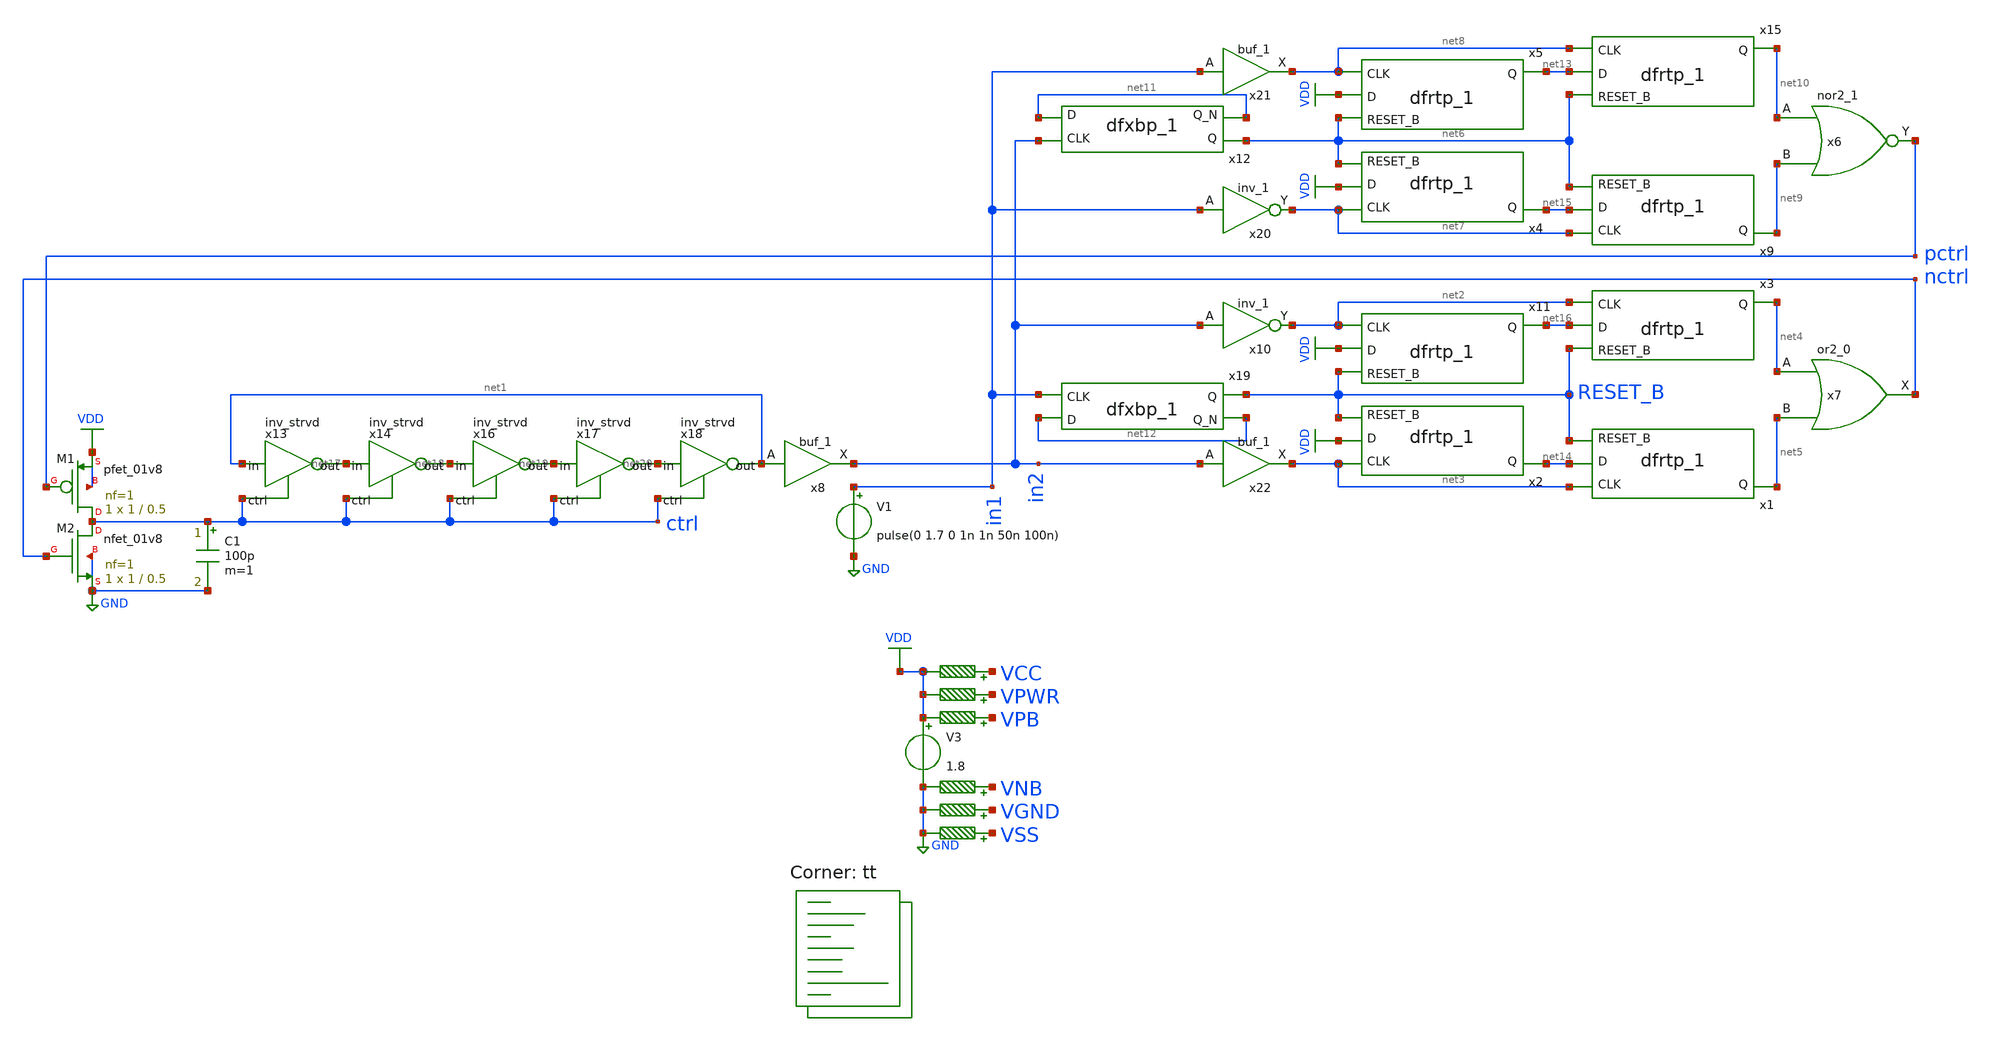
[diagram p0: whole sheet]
** sch_path: freq_det.sch
**.subckt freq_det
V3 VDD GND 1.8
R1 VNB GND 0.01 m=1
R2 VPB VDD 0.01 m=1
R3 VPWR VDD 0.01 m=1
R4 VGND GND 0.01 m=1
R5 VSS GND 0.01 m=1
R6 VCC VDD 0.01 m=1
V1 in1 GND pulse(0 1.7 0 1n 1n 50n 100n)
x13 net1 net17 ctrl VDD GND inv_strvd
x14 net17 net18 ctrl VDD GND inv_strvd
x16 net18 net19 ctrl VDD GND inv_strvd
x17 net19 net20 ctrl VDD GND inv_strvd
x18 net20 net1 ctrl VDD GND inv_strvd
XM1 ctrl pctrl VDD VDD sky130_fd_pr__pfet_01v8 L=0.5 W=1 nf=1 ad='int((nf+1)/2) * W/nf * 0.29' as='int((nf+2)/2) * W/nf * 0.29'
+ pd='2*int((nf+1)/2) * (W/nf + 0.29)' ps='2*int((nf+2)/2) * (W/nf + 0.29)' nrd='0.29 / W' nrs='0.29 / W'
+ sa=0 sb=0 sd=0 mult=1 m=1
XM2 ctrl nctrl GND GND sky130_fd_pr__nfet_01v8 L=0.5 W=1 nf=1 ad='int((nf+1)/2) * W/nf * 0.29' as='int((nf+2)/2) * W/nf * 0.29'
+ pd='2*int((nf+1)/2) * (W/nf + 0.29)' ps='2*int((nf+2)/2) * (W/nf + 0.29)' nrd='0.29 / W' nrs='0.29 / W'
+ sa=0 sb=0 sd=0 mult=1 m=1
C1 ctrl GND 100p m=1
x8 net1 VGND VNB VPB VPWR in2 sky130_fd_sc_hd__buf_1
x1 net3 net14 RESET_B VGND VNB VPB VPWR net5 sky130_fd_sc_hd__dfrtp_1
x7 net4 net5 VGND VNB VPB VPWR nctrl sky130_fd_sc_hd__or2_0
x15 net8 net13 net6 VGND VNB VPB VPWR net10 sky130_fd_sc_hd__dfrtp_1
x12 in2 net11 VGND VNB VPB VPWR net6 net11 sky130_fd_sc_hd__dfxbp_1
x19 in1 net12 VGND VNB VPB VPWR RESET_B net12 sky130_fd_sc_hd__dfxbp_1
x6 net10 net9 VGND VNB VPB VPWR pctrl sky130_fd_sc_hd__nor2_1
x10 in2 VGND VNB VPB VPWR net2 sky130_fd_sc_hd__inv_1
x20 in1 VGND VNB VPB VPWR net7 sky130_fd_sc_hd__inv_1
x3 net2 net16 RESET_B VGND VNB VPB VPWR net4 sky130_fd_sc_hd__dfrtp_1
x9 net7 net15 net6 VGND VNB VPB VPWR net9 sky130_fd_sc_hd__dfrtp_1
x2 net3 VDD RESET_B VGND VNB VPB VPWR net14 sky130_fd_sc_hd__dfrtp_1
x4 net7 VDD net6 VGND VNB VPB VPWR net15 sky130_fd_sc_hd__dfrtp_1
x5 net8 VDD net6 VGND VNB VPB VPWR net13 sky130_fd_sc_hd__dfrtp_1
x11 net2 VDD RESET_B VGND VNB VPB VPWR net16 sky130_fd_sc_hd__dfrtp_1
x21 in1 VGND VNB VPB VPWR net8 sky130_fd_sc_hd__buf_1
x22 in2 VGND VNB VPB VPWR net3 sky130_fd_sc_hd__buf_1
**** begin user architecture code
.lib $::SKYWATER_MODELS/sky130.lib.spice tt


.include /usr/local/share/pdk/sky130A/libs.ref/sky130_fd_sc_hd/spice/sky130_fd_sc_hd.spice tt
.control
  save all
  tran .1n 250m
  write top.raw
  quit 0
.endc


**** end user architecture code
**.ends

* expanding   symbol:  tt_um_wulf_8bit_vco/xschem/lib/inv_strvd.sym # of pins=3
** sym_path: archive/tt_um_wulf_8bit_vco/xschem/lib/inv_strvd.sym
** sch_path: archive/tt_um_wulf_8bit_vco/xschem/lib/inv_strvd.sch
.subckt inv_strvd in out ctrl VDD VSS
*.ipin in
*.ipin ctrl
*.opin out
XM2 out in net1 net1 sky130_fd_pr__nfet_01v8 L=1 W=40 nf=1 ad='int((1 + 1)/2) * 40 / 1 * 0.29' as='int((1 + 2)/2) * 40 / 1 * 0.29'
+ pd='2*int((1 + 1)/2) * (40 / 1 + 0.29)' ps='2*int((1 + 2)/2) * (40 / 1 + 0.29)' nrd='0.29 / 40 ' nrs='0.29 / 40 '
+ sa=0 sb=0 sd=0 mult=1 m=1
XM3 net1 ctrl VSS VSS sky130_fd_pr__nfet_01v8 L=0.15 W=1 nf=1 ad='int((1 + 1)/2) * 1 / 1 * 0.29' as='int((1 + 2)/2) * 1 / 1 * 0.29'
+ pd='2*int((1 + 1)/2) * (1 / 1 + 0.29)' ps='2*int((1 + 2)/2) * (1 / 1 + 0.29)' nrd='0.29 / 1 ' nrs='0.29 / 1 '
+ sa=0 sb=0 sd=0 mult=1 m=1
XM1 out in VDD VDD sky130_fd_pr__pfet_01v8 L=4 W=40 nf=1 ad='int((nf+1)/2) * W/nf * 0.29' as='int((nf+2)/2) * W/nf * 0.29'
+ pd='2*int((nf+1)/2) * (W/nf + 0.29)' ps='2*int((nf+2)/2) * (W/nf + 0.29)' nrd='0.29 / W' nrs='0.29 / W'
+ sa=0 sb=0 sd=0 mult=1 m=1
.ends

.GLOBAL GND
.GLOBAL VDD
.end
